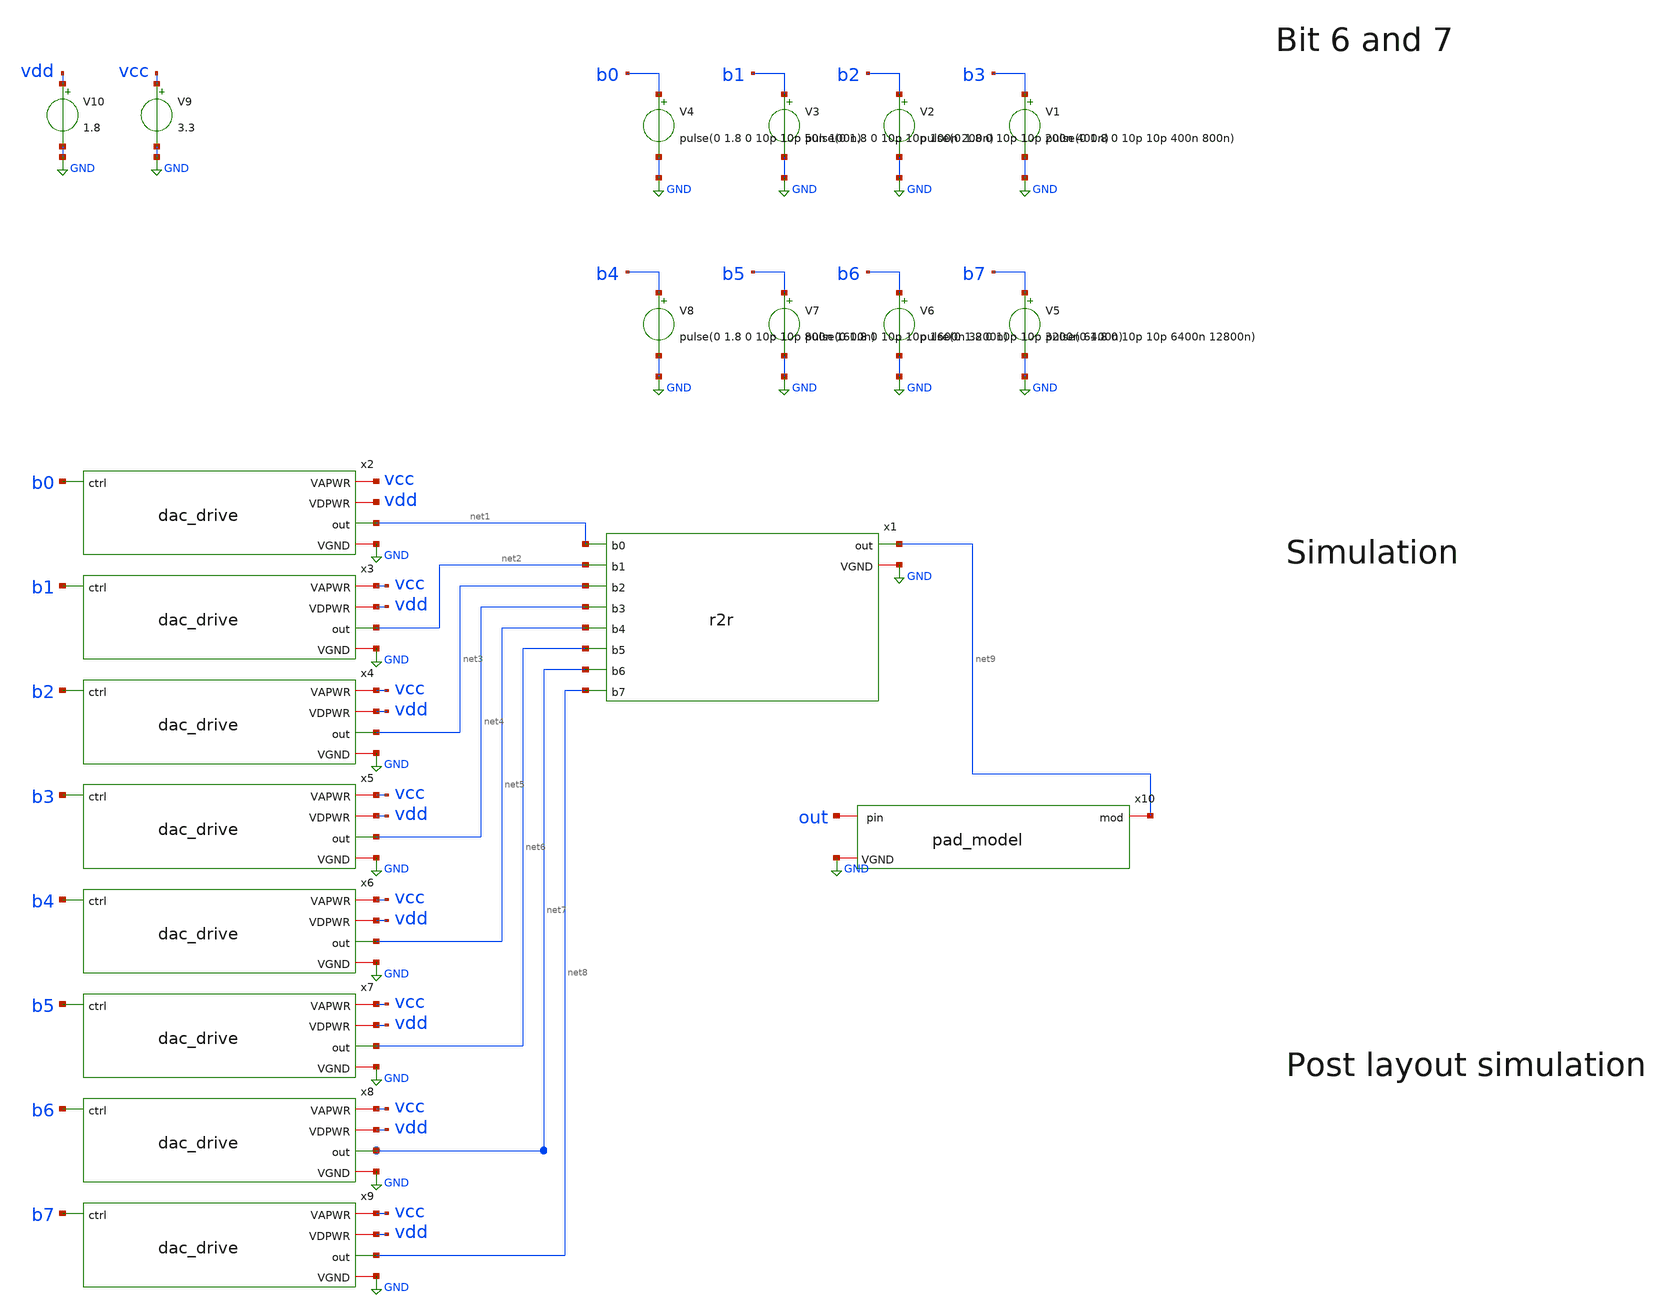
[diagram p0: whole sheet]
** sch_path: xschem/tb_dac.sch
**.subckt tb_dac
x1 net5 net3 net2 net1 net6 net7 net8 net4 net9 GND r2r
V1 b3 GND pulse(0 1.8 0 10p 10p 400n 800n)
V2 b2 GND pulse(0 1.8 0 10p 10p 200n 400n)
V3 b1 GND pulse(0 1.8 0 10p 10p 100n 200n)
V4 b0 GND pulse(0 1.8 0 10p 10p 50n 100n)
V5 b7 GND pulse(0 1.8 0 10p 10p 6400n 12800n)
V6 b6 GND pulse(0 1.8 0 10p 10p 3200n 6400n)
V7 b5 GND pulse(0 1.8 0 10p 10p 1600n 3200n)
V8 b4 GND pulse(0 1.8 0 10p 10p 800n 1600n)
x2 vcc vdd b0 net1 GND dac_drive
x3 vcc vdd b1 net2 GND dac_drive
x4 vcc vdd b2 net3 GND dac_drive
x5 vcc vdd b3 net4 GND dac_drive
x6 vcc vdd b4 net5 GND dac_drive
x7 vcc vdd b5 net6 GND dac_drive
x8 vcc vdd b6 net7 GND dac_drive
x9 vcc vdd b7 net8 GND dac_drive
V9 vcc GND 3.3
V10 vdd GND 1.8
x10 GND out net9 pad_model
**** begin user architecture code

** opencircuitdesign pdks install
.lib $::SKYWATER_MODELS/sky130.lib.spice tt




* .options filetype=ascii
.control
*tran 1n 128n uic
tran 1n 14000n uic
write tb_dac.raw
.endc
.end


**** end user architecture code
**.ends

* expanding   symbol:  r2r.sym # of pins=10
** sym_path: xschem/r2r.sym
** sch_path: xschem/r2r.sch
.subckt r2r b4 b2 b1 b0 b5 b6 b7 b3 out VGND
*.ipin b0
*.ipin b1
*.ipin b2
*.ipin b3
*.ipin b4
*.ipin b5
*.ipin b6
*.ipin b7
*.opin out
*.iopin VGND
XR1 net1 b0 VGND sky130_fd_pr__res_high_po_1p41 L=45 mult=1 m=1
XR7 net2 b1 VGND sky130_fd_pr__res_high_po_1p41 L=45 mult=1 m=1
XR10 net3 b2 VGND sky130_fd_pr__res_high_po_1p41 L=45 mult=1 m=1
XR13 net4 b3 VGND sky130_fd_pr__res_high_po_1p41 L=45 mult=1 m=1
XR16 net5 b4 VGND sky130_fd_pr__res_high_po_1p41 L=45 mult=1 m=1
XR19 net6 b5 VGND sky130_fd_pr__res_high_po_1p41 L=45 mult=1 m=1
XR22 net7 b6 VGND sky130_fd_pr__res_high_po_1p41 L=45 mult=1 m=1
XR25 net8 b7 VGND sky130_fd_pr__res_high_po_1p41 L=45 mult=1 m=1
XR5 b a VGND sky130_fd_pr__res_high_po_1p41 L=45 mult=1 m=1
XR8 c b VGND sky130_fd_pr__res_high_po_1p41 L=45 mult=1 m=1
XR11 d c VGND sky130_fd_pr__res_high_po_1p41 L=45 mult=1 m=1
XR14 e d VGND sky130_fd_pr__res_high_po_1p41 L=45 mult=1 m=1
XR17 f e VGND sky130_fd_pr__res_high_po_1p41 L=45 mult=1 m=1
XR20 g f VGND sky130_fd_pr__res_high_po_1p41 L=45 mult=1 m=1
XR23 out g VGND sky130_fd_pr__res_high_po_1p41 L=45 mult=1 m=1
XR3 net9 a VGND sky130_fd_pr__res_high_po_1p41 L=45 mult=1 m=1
XR2 a net1 VGND sky130_fd_pr__res_high_po_1p41 L=45 mult=1 m=1
XR6 b net2 VGND sky130_fd_pr__res_high_po_1p41 L=45 mult=1 m=1
XR9 c net3 VGND sky130_fd_pr__res_high_po_1p41 L=45 mult=1 m=1
XR12 d net4 VGND sky130_fd_pr__res_high_po_1p41 L=45 mult=1 m=1
XR15 e net5 VGND sky130_fd_pr__res_high_po_1p41 L=45 mult=1 m=1
XR18 f net6 VGND sky130_fd_pr__res_high_po_1p41 L=45 mult=1 m=1
XR21 g net7 VGND sky130_fd_pr__res_high_po_1p41 L=45 mult=1 m=1
XR24 out net8 VGND sky130_fd_pr__res_high_po_1p41 L=45 mult=1 m=1
XR4 VGND net9 VGND sky130_fd_pr__res_high_po_1p41 L=45 mult=1 m=1
XR26 VGND VGND VGND sky130_fd_pr__res_high_po_1p41 L=45 mult=1 m=1
XR27 VGND VGND VGND sky130_fd_pr__res_high_po_1p41 L=45 mult=1 m=1
.ends


* expanding   symbol:  dac_drive.sym # of pins=5
** sym_path: xschem/dac_drive.sym
** sch_path: xschem/dac_drive.sch
.subckt dac_drive VAPWR VDPWR ctrl out VGND
*.ipin ctrl
*.iopin VGND
*.iopin VDPWR
*.iopin VAPWR
*.opin out
XM8 ctrl_n ctrl VDPWR VDPWR sky130_fd_pr__pfet_01v8_hvt L=0.15 W=1 nf=1 ad='int((nf+1)/2) * W/nf * 0.29'
+ as='int((nf+2)/2) * W/nf * 0.29' pd='2*int((nf+1)/2) * (W/nf + 0.29)' ps='2*int((nf+2)/2) * (W/nf + 0.29)'
+ nrd='0.29 / W' nrs='0.29 / W' sa=0 sb=0 sd=0 mult=1 m=1
XM7 ctrl_n ctrl VGND VGND sky130_fd_pr__nfet_01v8 L=0.15 W=0.42 nf=1 ad='int((nf+1)/2) * W/nf * 0.29'
+ as='int((nf+2)/2) * W/nf * 0.29' pd='2*int((nf+1)/2) * (W/nf + 0.29)' ps='2*int((nf+2)/2) * (W/nf + 0.29)'
+ nrd='0.29 / W' nrs='0.29 / W' sa=0 sb=0 sd=0 mult=1 m=1
XM11 m9m11 m10m12 VAPWR VAPWR sky130_fd_pr__pfet_g5v0d10v5 L=0.5 W=0.42 nf=1 ad='int((nf+1)/2) * W/nf * 0.29'
+ as='int((nf+2)/2) * W/nf * 0.29' pd='2*int((nf+1)/2) * (W/nf + 0.29)' ps='2*int((nf+2)/2) * (W/nf + 0.29)'
+ nrd='0.29 / W' nrs='0.29 / W' sa=0 sb=0 sd=0 mult=1 m=1
XM9 m9m11 ctrl VGND VGND sky130_fd_pr__nfet_g5v0d10v5 L=0.5 W=0.42 nf=1 ad='int((nf+1)/2) * W/nf * 0.29'
+ as='int((nf+2)/2) * W/nf * 0.29' pd='2*int((nf+1)/2) * (W/nf + 0.29)' ps='2*int((nf+2)/2) * (W/nf + 0.29)'
+ nrd='0.29 / W' nrs='0.29 / W' sa=0 sb=0 sd=0 mult=1 m=1
XM10 m10m12 ctrl_n VGND VGND sky130_fd_pr__nfet_g5v0d10v5 L=0.5 W=0.42 nf=1 ad='int((nf+1)/2) * W/nf * 0.29'
+ as='int((nf+2)/2) * W/nf * 0.29' pd='2*int((nf+1)/2) * (W/nf + 0.29)' ps='2*int((nf+2)/2) * (W/nf + 0.29)'
+ nrd='0.29 / W' nrs='0.29 / W' sa=0 sb=0 sd=0 mult=1 m=1
XM12 m10m12 m9m11 VAPWR VAPWR sky130_fd_pr__pfet_g5v0d10v5 L=0.5 W=0.42 nf=1 ad='int((nf+1)/2) * W/nf * 0.29'
+ as='int((nf+2)/2) * W/nf * 0.29' pd='2*int((nf+1)/2) * (W/nf + 0.29)' ps='2*int((nf+2)/2) * (W/nf + 0.29)'
+ nrd='0.29 / W' nrs='0.29 / W' sa=0 sb=0 sd=0 mult=1 m=1
XM1 out_drive m10m12 VAPWR VAPWR sky130_fd_pr__pfet_g5v0d10v5 L=0.5 W=0.84 nf=1 ad='int((nf+1)/2) * W/nf * 0.29'
+ as='int((nf+2)/2) * W/nf * 0.29' pd='2*int((nf+1)/2) * (W/nf + 0.29)' ps='2*int((nf+2)/2) * (W/nf + 0.29)'
+ nrd='0.29 / W' nrs='0.29 / W' sa=0 sb=0 sd=0 mult=1 m=1
XM2 out_drive m10m12 VGND VGND sky130_fd_pr__nfet_g5v0d10v5 L=0.5 W=0.42 nf=1 ad='int((nf+1)/2) * W/nf * 0.29'
+ as='int((nf+2)/2) * W/nf * 0.29' pd='2*int((nf+1)/2) * (W/nf + 0.29)' ps='2*int((nf+2)/2) * (W/nf + 0.29)'
+ nrd='0.29 / W' nrs='0.29 / W' sa=0 sb=0 sd=0 mult=1 m=1
XM3 out out_drive VAPWR VAPWR sky130_fd_pr__pfet_g5v0d10v5 L=0.5 W=9 nf=3 ad='int((nf+1)/2) * W/nf * 0.29'
+ as='int((nf+2)/2) * W/nf * 0.29' pd='2*int((nf+1)/2) * (W/nf + 0.29)' ps='2*int((nf+2)/2) * (W/nf + 0.29)'
+ nrd='0.29 / W' nrs='0.29 / W' sa=0 sb=0 sd=0 mult=1 m=1
XM4 out out_drive VGND VGND sky130_fd_pr__nfet_g5v0d10v5 L=0.5 W=3 nf=1 ad='int((nf+1)/2) * W/nf * 0.29'
+ as='int((nf+2)/2) * W/nf * 0.29' pd='2*int((nf+1)/2) * (W/nf + 0.29)' ps='2*int((nf+2)/2) * (W/nf + 0.29)'
+ nrd='0.29 / W' nrs='0.29 / W' sa=0 sb=0 sd=0 mult=1 m=1
.ends


* expanding   symbol:  pad_model.sym # of pins=3
** sym_path: xschem/pad_model.sym
** sch_path: xschem/pad_model.sch
.subckt pad_model VGND pin mod
*.iopin pin
*.iopin mod
*.iopin VGND
XM1 net3 VAPWR mod VGND sky130_fd_pr__nfet_g5v0d10v5 L=0.5 W=60 nf=12 ad='int((nf+1)/2) * W/nf * 0.29'
+ as='int((nf+2)/2) * W/nf * 0.29' pd='2*int((nf+1)/2) * (W/nf + 0.29)' ps='2*int((nf+2)/2) * (W/nf + 0.29)'
+ nrd='0.29 / W' nrs='0.29 / W' sa=0 sb=0 sd=0 mult=1 m=1
XM2 net3 VGND mod VAPWR sky130_fd_pr__pfet_g5v0d10v5 L=0.5 W=180 nf=18 ad='int((nf+1)/2) * W/nf * 0.29'
+ as='int((nf+2)/2) * W/nf * 0.29' pd='2*int((nf+1)/2) * (W/nf + 0.29)' ps='2*int((nf+2)/2) * (W/nf + 0.29)'
+ nrd='0.29 / W' nrs='0.29 / W' sa=0 sb=0 sd=0 mult=1 m=1
C1 pin VGND 2p m=1
V1 VAPWR VGND 3.3
R1 net1 pin 1 m=1
L1 net2 net1 1n m=1
C2 net2 VGND 3p m=1
R2 net3 net2 50 m=1
C3 mod VGND 250f m=1
XM3 net3 VGND VGND VGND sky130_fd_pr__nfet_g5v0d10v5 L=0.5 W=60 nf=12 ad='int((nf+1)/2) * W/nf * 0.29'
+ as='int((nf+2)/2) * W/nf * 0.29' pd='2*int((nf+1)/2) * (W/nf + 0.29)' ps='2*int((nf+2)/2) * (W/nf + 0.29)'
+ nrd='0.29 / W' nrs='0.29 / W' sa=0 sb=0 sd=0 mult=15 m=15
XM4 net3 VAPWR VGND VAPWR sky130_fd_pr__pfet_g5v0d10v5 L=0.5 W=180 nf=18 ad='int((nf+1)/2) * W/nf * 0.29'
+ as='int((nf+2)/2) * W/nf * 0.29' pd='2*int((nf+1)/2) * (W/nf + 0.29)' ps='2*int((nf+2)/2) * (W/nf + 0.29)'
+ nrd='0.29 / W' nrs='0.29 / W' sa=0 sb=0 sd=0 mult=15 m=15
.ends

.GLOBAL GND
.end
